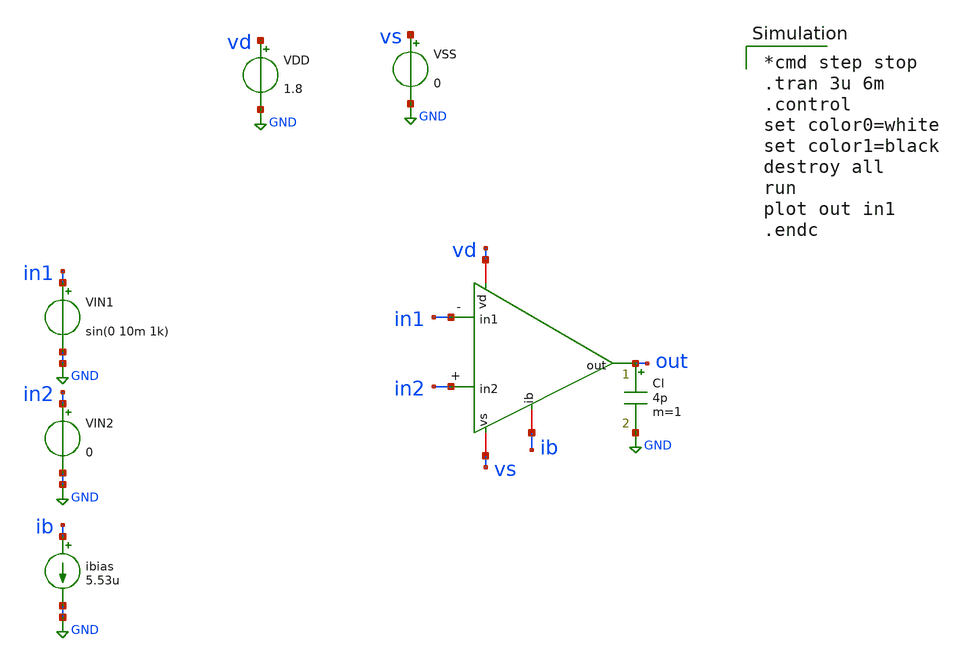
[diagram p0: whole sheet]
** sch_path: amp-op/xschem/ampop_tb-tran.sch
* Copyright 2020 Stefan Frederik Schippers
* Licensed under the Apache License, Version 2.0 (the "License");
* you may not use this file except in compliance with the License.
* You may obtain a copy of the License at
* https://www.apache.org/licenses/LICENSE-2.0
* Unless required by applicable law or agreed to in writing, software
* distributed under the License is distributed on an "AS IS" BASIS,
* WITHOUT WARRANTIES OR CONDITIONS OF ANY KIND, either express or implied.
* See the License for the specific language governing permissions and
* limitations under the License.
**.subckt ampop_tb-tran
VIN2 in2 GND 0
VIN1 in1 GND sin(0 10m 1k)
ibias ib GND 5.53u
VDD vd GND 1.8
VSS vs GND 0
Cl out GND 4p m=1
x1 vd in1 in2 out ib vs ampop
**** begin user architecture code

*cmd step stop
.tran 3u 6m
.control
set color0=white
set color1=black
destroy all
run
plot out in1
.endc

 .lib $::SKYWATER_MODELS/sky130.lib.spice tt
.include $::SKYWATER_STDCELLS/sky130_fd_sc_hd.spice

**** end user architecture code
**.ends

* expanding   symbol:  /home/hugodg/projects-sky130/temp-sensor/amp-op/xschem/ampop.sym # of pins=6
** sym_path: amp-op/xschem/ampop.sym
** sch_path: amp-op/xschem/ampop.sch
.subckt ampop vd in1 in2 out ib vs
*.iopin vd
*.opin out
*.ipin in1
*.ipin in2
*.iopin vs
*.iopin ib
X1 vd net1 out ib vs buffer
X2 vd ib net1 in2 in1 vs ota
**** begin user architecture code


R0 in1 in1.t0 88.243
R1 in2 in2.t0 88.786
R2 vs.n0 vs.n4 362.164
R3 vs.n0 vs.n2 362.164
R4 vs.n30 vs.n25 181.834
R5 vs.n14 vs.n9 181.834
R6 vs.n18 vs.n17 108.422
R7 vs.n31 vs.n30 108.422
R8 vs.n0 vs.n6 108.422
R9 vs.n15 vs.n14 108.422
R10 vs.n34 vs.n5 5.045
R11 vs.n5 vs 0.812
R12 vs vs 0.431
R13 vs.n34 vs.n33 0.202
R14 vs vs.n34 0.182
R15 vs.n19 vs.n16 0.15
R16 vs.n32 vs.n23 0.062
R17 vs.n20 vs.n19 0.057
R18 vs.n16 vs.n7 0.055
R19 vs.n25 vs.n24 0.046
R20 vs.n9 vs.n8 0.046
R21 vs.n30 vs.n29 0.042
R22 vs.n14 vs.n13 0.042
R23 vs.n28 vs.n27 0.035
R24 vs.n12 vs.n11 0.035
R25 vs.n27 vs.n26 0.025
R26 vs.n11 vs.n10 0.025
R27 vs.n29 vs.n28 0.025
R28 vs.n13 vs.n12 0.025
R29 vs.n16 vs.n15 0.017
R30 vs.n19 vs.n18 0.017
R31 vs.n32 vs.n31 0.017
R32 vs.n4 vs.n3 0.013
R33 vs.n2 vs.n1 0.013
R34 vs.n7 vs.n0 0.007
R35 vs vs 0.005
R36 vs.n23 vs.n20 0.004
R37 vs.n33 vs.n32 0.003
R38 vs.n5 vs 0.002
R39 vs.n22 vs.n21 0.001
R40 vs.n23 vs.n22 0.001
R41 ib.n5 ib.t6 196.205
R42 ib.n6 ib.t5 196.185
R43 ib.n7 ib.t8 196.183
R44 ib.n8 ib.t7 196.181
R45 ib.n4 ib.t2 160.591
R46 ib.t2 ib.n3 160.08
R47 ib.n4 ib.t4 160.055
R48 ib.n0 ib.t9 24.837
R49 ib.n0 ib.t0 24.107
R50 ib.n1 ib.t1 17.747
R51 ib.n3 ib.t3 5.789
R52 ib.n2 ib.n1 4.041
R53 ib ib.n8 3.3
R54 ib.n5 ib.n4 1.125
R55 ib.n3 ib 0.407
R56 ib.n1 ib.n0 0.387
R57 ib.n6 ib.n5 0.175
R58 ib.n8 ib.n7 0.168
R59 ib.n7 ib.n6 0.162
R60 ib.n2 ib 0.113
R61 ib ib.n2 0.078
R62 vd.n74 vd.n73 5396.47
R63 vd.n63 vd.n62 3501.18
R64 vd.n84 vd.n83 3501.18
R65 vd.n62 vd.n59 909.81
R66 vd.n83 vd.n80 909.81
R67 vd.n65 vd.n64 722.167
R68 vd.n86 vd.n85 722.167
R69 vd.n71 vd.n70 575.623
R70 vd.n75 vd.n70 575.623
R71 vd.n74 vd.n69 569.784
R72 vd.n72 vd.n71 515.374
R73 vd.n53 vd.n52 379.482
R74 vd.n40 vd.n34 379.482
R75 vd.n61 vd.n60 373.458
R76 vd.n65 vd.n60 373.458
R77 vd.n82 vd.n81 373.458
R78 vd.n86 vd.n81 373.458
R79 vd.n69 vd.n68 326.776
R80 vd.n54 vd.n53 297.411
R81 vd.n41 vd.n40 297.411
R82 vd.n59 vd.n58 270.305
R83 vd.n80 vd.n79 270.305
R84 vd.n76 vd.n75 251.205
R85 vd.n71 vd.n68 248.846
R86 vd.n19 vd.n16 131.387
R87 vd.n4 vd.n1 131.387
R88 vd.n24 vd.n21 131.011
R89 vd.n9 vd.n6 131.011
R90 vd.n66 vd.n65 105.107
R91 vd.n87 vd.n86 105.107
R92 vd.n61 vd.n58 103.152
R93 vd.n82 vd.n79 103.152
R94 vd.n29 vd.n24 54.211
R95 vd.n14 vd.n9 54.211
R96 vd.n29 vd.n19 53.835
R97 vd.n14 vd.n4 53.835
R98 vd.n57 vd.n14 8.271
R99 vd.n57 vd.n29 7.938
R100 vd.n57 vd.n56 4.028
R101 vd.n91 vd.n90 1.897
R102 vd.n77 vd.n76 1.606
R103 vd.n67 vd.n66 1.199
R104 vd.n88 vd.n87 1.199
R105 vd.n91 vd.n57 1.058
R106 vd vd.n89 1.008
R107 vd.n78 vd.n77 0.975
R108 vd vd.n88 0.594
R109 vd.n77 vd.n68 0.389
R110 vd.n67 vd.n58 0.389
R111 vd.n88 vd.n79 0.334
R112 vd.n55 vd.n45 0.296
R113 vd.n89 vd.n78 0.273
R114 vd.n42 vd.n32 0.228
R115 vd.n56 vd.n55 0.18
R116 vd.n89 vd 0.173
R117 vd.n56 vd.n42 0.167
R118 vd.n19 vd.n18 0.161
R119 vd.n24 vd.n23 0.161
R120 vd.n4 vd.n3 0.161
R121 vd.n9 vd.n8 0.161
R122 vd.n23 vd.n22 0.139
R123 vd.n8 vd.n7 0.139
R124 vd.n18 vd.n17 0.139
R125 vd.n3 vd.n2 0.139
R126 vd.n90 vd 0.071
R127 vd.n78 vd.n67 0.054
R128 vd vd.n91 0.044
R129 vd.n90 vd 0.034
R130 vd.n42 vd.n41 0.017
R131 vd.n55 vd.n54 0.017
R132 vd.n62 vd.n61 0.015
R133 vd.n83 vd.n82 0.015
R134 vd.n16 vd.n15 0.015
R135 vd.n21 vd.n20 0.015
R136 vd.n1 vd.n0 0.015
R137 vd.n6 vd.n5 0.015
R138 vd.n52 vd.n51 0.013
R139 vd.n34 vd.n33 0.013
R140 vd.n26 vd.n25 0.013
R141 vd.n27 vd.n26 0.013
R142 vd.n11 vd.n10 0.013
R143 vd.n12 vd.n11 0.013
R144 vd.n75 vd.n74 0.004
R145 vd.n73 vd.n72 0.003
R146 vd.n63 vd.n60 0.003
R147 vd.n84 vd.n81 0.003
R148 vd.n53 vd.n50 0.003
R149 vd.n47 vd.n46 0.003
R150 vd.n36 vd.n35 0.003
R151 vd.n40 vd.n39 0.003
R152 vd.n64 vd.n63 0.003
R153 vd.n85 vd.n84 0.003
R154 vd.n50 vd.n49 0.003
R155 vd.n37 vd.n36 0.003
R156 vd.n48 vd.n47 0.003
R157 vd.n39 vd.n38 0.003
R158 vd.n73 vd.n70 0.003
R159 vd.n49 vd.n48 0.002
R160 vd.n38 vd.n37 0.002
R161 vd.n29 vd.n28 0.002
R162 vd.n28 vd.n27 0.002
R163 vd.n14 vd.n13 0.002
R164 vd.n13 vd.n12 0.002
R165 vd.n72 vd.n69 0.001
R166 vd.n64 vd.n59 0.001
R167 vd.n85 vd.n80 0.001
R168 vd.n32 vd.n31 0.001
R169 vd.n45 vd.n44 0.001
R170 vd.n44 vd.n43 0.001
R171 vd.n31 vd.n30 0.001
R172 vd.n76 vd.n69 0.001
R173 vd.n66 vd.n59 0.001
R174 vd.n87 vd.n80 0.001
R175 out.t0 out.n7 175.091
R176 out.n0 out.t2 175.044
R177 out.n2 out.n1 150.491
R178 out.n4 out.n3 150.491
R179 out.n6 out.n5 141.106
R180 out out.t0 28.743
R181 out.n5 out.t1 24.103
R182 out.n6 out.t7 24.103
R183 out.n4 out.t5 24.103
R184 out.n2 out.t3 24.102
R185 out.n0 out.t6 24.102
R186 out.n1 out.t9 24.102
R187 out.n3 out.t4 24.102
R188 out.n7 out.t8 24.102
R189 out.n7 out.n6 1.085
R190 out.n3 out.n2 0.988
R191 out.n5 out.n4 0.913
R192 out.n1 out.n0 0.863
R193 out out 0.023
R194 buffer_0/net1.n4 buffer_0/net1.t29 172.218
R195 buffer_0/net1.n5 buffer_0/net1.n4 149.523
R196 buffer_0/net1.n6 buffer_0/net1.n5 149.523
R197 buffer_0/net1.n7 buffer_0/net1.n6 149.523
R198 buffer_0/net1.n8 buffer_0/net1.n7 149.523
R199 buffer_0/net1.n9 buffer_0/net1.n8 149.523
R200 buffer_0/net1.n10 buffer_0/net1.n9 149.523
R201 buffer_0/net1.n11 buffer_0/net1.n10 149.523
R202 buffer_0/net1.n12 buffer_0/net1.n11 149.523
R203 buffer_0/net1.n13 buffer_0/net1.n12 149.523
R204 buffer_0/net1.n14 buffer_0/net1.n13 149.523
R205 buffer_0/net1.n15 buffer_0/net1.n14 149.523
R206 buffer_0/net1.n16 buffer_0/net1.n15 149.523
R207 buffer_0/net1.n17 buffer_0/net1.n16 149.523
R208 buffer_0/net1.n18 buffer_0/net1.n17 149.523
R209 buffer_0/net1.n19 buffer_0/net1.n18 149.523
R210 buffer_0/net1.n20 buffer_0/net1.n19 149.523
R211 buffer_0/net1.n21 buffer_0/net1.n20 149.523
R212 buffer_0/net1.n22 buffer_0/net1.n21 148.639
R213 buffer_0/net1.n22 buffer_0/net1.t16 24.284
R214 buffer_0/net1.n21 buffer_0/net1.t10 24.101
R215 buffer_0/net1.n20 buffer_0/net1.t27 24.101
R216 buffer_0/net1.n19 buffer_0/net1.t21 24.101
R217 buffer_0/net1.n18 buffer_0/net1.t4 24.101
R218 buffer_0/net1.n17 buffer_0/net1.t0 24.101
R219 buffer_0/net1.n16 buffer_0/net1.t22 24.101
R220 buffer_0/net1.n15 buffer_0/net1.t26 24.101
R221 buffer_0/net1.n14 buffer_0/net1.t18 24.101
R222 buffer_0/net1.n13 buffer_0/net1.t6 24.101
R223 buffer_0/net1.n12 buffer_0/net1.t23 24.101
R224 buffer_0/net1.n11 buffer_0/net1.t25 24.101
R225 buffer_0/net1.n10 buffer_0/net1.t8 24.101
R226 buffer_0/net1.n9 buffer_0/net1.t12 24.101
R227 buffer_0/net1.n8 buffer_0/net1.t28 24.101
R228 buffer_0/net1.n7 buffer_0/net1.t24 24.101
R229 buffer_0/net1.n6 buffer_0/net1.t14 24.101
R230 buffer_0/net1.n5 buffer_0/net1.t2 24.101
R231 buffer_0/net1.n4 buffer_0/net1.t20 24.101
R232 buffer_0/net1.n3 buffer_0/net1.t11 17.4
R233 buffer_0/net1.n3 buffer_0/net1.t17 17.4
R234 buffer_0/net1.n0 buffer_0/net1.t3 17.4
R235 buffer_0/net1.n0 buffer_0/net1.t15 17.4
R236 buffer_0/net1.n1 buffer_0/net1.t13 17.4
R237 buffer_0/net1.n1 buffer_0/net1.t9 17.4
R238 buffer_0/net1.n2 buffer_0/net1.t1 17.4
R239 buffer_0/net1.n2 buffer_0/net1.t5 17.4
R240 buffer_0/net1.n25 buffer_0/net1.t7 17.4
R241 buffer_0/net1.n25 buffer_0/net1.t19 17.4
R242 buffer_0/net1.n24 buffer_0/net1.n23 3.481
R243 buffer_0/net1 buffer_0/net1.n0 3.306
R244 buffer_0/net1.n27 buffer_0/net1.n26 3.218
R245 buffer_0/net1.n26 buffer_0/net1.n24 3.218
R246 buffer_0/net1.n23 buffer_0/net1.n22 1.24
R247 buffer_0/net1.n27 buffer_0/net1.n1 0.931
R248 buffer_0/net1.n24 buffer_0/net1.n2 0.931
R249 buffer_0/net1.n26 buffer_0/net1.n25 0.931
R250 buffer_0/net1 buffer_0/net1.n27 0.843
R251 buffer_0/net1.n23 buffer_0/net1.n3 0.389
C0 ota_0/m1_1300_5200# ota_0/out -0.03fF
C1 buffer_0/net2 vd 0.01fF
C2 ota_0/out vd 0.05fF
C3 buffer_0/net1.t3 vs 0.02fF
C4 buffer_0/net1.t15 vs 0.02fF
C5 buffer_0/net1.n0 vs 0.31fF $ **FLOATING
C6 buffer_0/net1.t13 vs 0.02fF
C7 buffer_0/net1.t9 vs 0.02fF
C8 buffer_0/net1.n1 vs 0.19fF $ **FLOATING
C9 buffer_0/net1.t1 vs 0.02fF
C10 buffer_0/net1.t5 vs 0.02fF
C11 buffer_0/net1.n2 vs 0.19fF $ **FLOATING
C12 buffer_0/net1.t11 vs 0.02fF
C13 buffer_0/net1.t17 vs 0.02fF
C14 buffer_0/net1.n3 vs 0.15fF $ **FLOATING
C15 buffer_0/net1.t10 vs 0.47fF
C16 buffer_0/net1.t27 vs 0.47fF
C17 buffer_0/net1.t21 vs 0.47fF
C18 buffer_0/net1.t4 vs 0.47fF
C19 buffer_0/net1.t0 vs 0.47fF
C20 buffer_0/net1.t22 vs 0.47fF
C21 buffer_0/net1.t26 vs 0.47fF
C22 buffer_0/net1.t18 vs 0.47fF
C23 buffer_0/net1.t6 vs 0.47fF
C24 buffer_0/net1.t23 vs 0.47fF
C25 buffer_0/net1.t25 vs 0.47fF
C26 buffer_0/net1.t8 vs 0.47fF
C27 buffer_0/net1.t12 vs 0.47fF
C28 buffer_0/net1.t28 vs 0.47fF
C29 buffer_0/net1.t24 vs 0.47fF
C30 buffer_0/net1.t14 vs 0.47fF
C31 buffer_0/net1.t2 vs 0.47fF
C32 buffer_0/net1.t20 vs 0.47fF
C33 buffer_0/net1.t29 vs 0.75fF
C34 buffer_0/net1.n4 vs 0.39fF $ **FLOATING
C35 buffer_0/net1.n5 vs 0.34fF $ **FLOATING
C36 buffer_0/net1.n6 vs 0.34fF $ **FLOATING
C37 buffer_0/net1.n7 vs 0.34fF $ **FLOATING
C38 buffer_0/net1.n8 vs 0.34fF $ **FLOATING
C39 buffer_0/net1.n9 vs 0.34fF $ **FLOATING
C40 buffer_0/net1.n10 vs 0.34fF $ **FLOATING
C41 buffer_0/net1.n11 vs 0.34fF $ **FLOATING
C42 buffer_0/net1.n12 vs 0.34fF $ **FLOATING
C43 buffer_0/net1.n13 vs 0.34fF $ **FLOATING
C44 buffer_0/net1.n14 vs 0.34fF $ **FLOATING
C45 buffer_0/net1.n15 vs 0.34fF $ **FLOATING
C46 buffer_0/net1.n16 vs 0.34fF $ **FLOATING
C47 buffer_0/net1.n17 vs 0.34fF $ **FLOATING
C48 buffer_0/net1.n18 vs 0.34fF $ **FLOATING
C49 buffer_0/net1.n19 vs 0.34fF $ **FLOATING
C50 buffer_0/net1.n20 vs 0.34fF $ **FLOATING
C51 buffer_0/net1.n21 vs 0.34fF $ **FLOATING
C52 buffer_0/net1.t16 vs 0.47fF
C53 buffer_0/net1.n22 vs 0.21fF $ **FLOATING
C54 buffer_0/net1.n23 vs 1.22fF $ **FLOATING
C55 buffer_0/net1.n24 vs 4.35fF $ **FLOATING
C56 buffer_0/net1.t7 vs 0.02fF
C57 buffer_0/net1.t19 vs 0.02fF
C58 buffer_0/net1.n25 vs 0.19fF $ **FLOATING
C59 buffer_0/net1.n26 vs 0.36fF $ **FLOATING
C60 buffer_0/net1.n27 vs 0.25fF $ **FLOATING
C61 out.t8 vs 0.59fF
C62 out.t1 vs 0.59fF
C63 out.t4 vs 0.59fF
C64 out.t9 vs 0.59fF
C65 out.t2 vs 0.94fF
C66 out.t6 vs 0.59fF
C67 out.n0 vs 2.69fF $ **FLOATING
C68 out.n1 vs 2.83fF $ **FLOATING
C69 out.t3 vs 0.59fF
C70 out.n2 vs 0.86fF $ **FLOATING
C71 out.n3 vs 0.86fF $ **FLOATING
C72 out.t5 vs 0.59fF
C73 out.n4 vs 0.91fF $ **FLOATING
C74 out.n5 vs 0.92fF $ **FLOATING
C75 out.t7 vs 0.59fF
C76 out.n6 vs 0.84fF $ **FLOATING
C77 out.n7 vs 0.91fF $ **FLOATING
C78 out.t0 vs 0.89fF
C79 vd.n0 vs 0.34fF $ **FLOATING
C80 vd.n1 vs 0.06fF $ **FLOATING
C81 vd.n2 vs 0.33fF $ **FLOATING
C82 vd.n3 vs 0.04fF $ **FLOATING
C83 vd.n4 vs 0.04fF $ **FLOATING
C84 vd.n5 vs 0.34fF $ **FLOATING
C85 vd.n6 vs 0.06fF $ **FLOATING
C86 vd.n7 vs 0.33fF $ **FLOATING
C87 vd.n8 vs 0.04fF $ **FLOATING
C88 vd.n9 vs 0.04fF $ **FLOATING
C89 vd.n10 vs 0.07fF $ **FLOATING
C90 vd.n11 vs 0.07fF $ **FLOATING
C91 vd.n12 vs 0.35fF $ **FLOATING
C92 vd.n13 vs 0.02fF $ **FLOATING
C93 vd.n14 vs 0.49fF $ **FLOATING
C94 vd.n15 vs 0.34fF $ **FLOATING
C95 vd.n16 vs 0.06fF $ **FLOATING
C96 vd.n17 vs 0.33fF $ **FLOATING
C97 vd.n18 vs 0.04fF $ **FLOATING
C98 vd.n19 vs 0.04fF $ **FLOATING
C99 vd.n20 vs 0.34fF $ **FLOATING
C100 vd.n21 vs 0.06fF $ **FLOATING
C101 vd.n22 vs 0.33fF $ **FLOATING
C102 vd.n23 vs 0.04fF $ **FLOATING
C103 vd.n24 vs 0.04fF $ **FLOATING
C104 vd.n25 vs 0.07fF $ **FLOATING
C105 vd.n26 vs 0.07fF $ **FLOATING
C106 vd.n27 vs 0.35fF $ **FLOATING
C107 vd.n28 vs 0.02fF $ **FLOATING
C108 vd.n29 vs 0.51fF $ **FLOATING
C109 vd.n30 vs 1.30fF $ **FLOATING
C110 vd.n31 vs 0.03fF $ **FLOATING
C111 vd.n32 vs 0.64fF $ **FLOATING
C112 vd.n33 vs 1.30fF $ **FLOATING
C113 vd.n34 vs 0.15fF $ **FLOATING
C114 vd.n35 vs 0.13fF $ **FLOATING
C115 vd.n36 vs 0.14fF $ **FLOATING
C116 vd.n37 vs 1.01fF $ **FLOATING
C117 vd.n38 vs 1.01fF $ **FLOATING
C118 vd.n39 vs 0.14fF $ **FLOATING
C119 vd.n40 vs 0.13fF $ **FLOATING
C120 vd.n41 vs 0.07fF $ **FLOATING
C121 vd.n42 vs 0.10fF $ **FLOATING
C122 vd.n43 vs 1.30fF $ **FLOATING
C123 vd.n44 vs 0.03fF $ **FLOATING
C124 vd.n45 vs 0.34fF $ **FLOATING
C125 vd.n46 vs 0.13fF $ **FLOATING
C126 vd.n47 vs 0.14fF $ **FLOATING
C127 vd.n48 vs 1.01fF $ **FLOATING
C128 vd.n49 vs 1.01fF $ **FLOATING
C129 vd.n50 vs 0.14fF $ **FLOATING
C130 vd.n51 vs 1.30fF $ **FLOATING
C131 vd.n52 vs 0.15fF $ **FLOATING
C132 vd.n53 vs 0.13fF $ **FLOATING
C133 vd.n54 vs 0.07fF $ **FLOATING
C134 vd.n55 vs 0.35fF $ **FLOATING
C135 vd.n56 vs 1.41fF $ **FLOATING
C136 vd.n57 vs 13.41fF $ **FLOATING
C137 vd.n58 vs 0.09fF $ **FLOATING
C138 vd.n59 vs 2.13fF $ **FLOATING
C139 vd.n60 vs 0.14fF $ **FLOATING
C140 vd.n61 vs 0.09fF $ **FLOATING
C141 vd.n62 vs 1.22fF $ **FLOATING
C142 vd.n63 vs 0.14fF $ **FLOATING
C143 vd.n65 vs 1.31fF $ **FLOATING
C144 vd.n66 vs 0.26fF $ **FLOATING
C145 vd.n67 vs 0.81fF $ **FLOATING
C146 vd.n68 vs 0.13fF $ **FLOATING
C147 vd.n69 vs 5.56fF $ **FLOATING
C148 vd.n70 vs 0.22fF $ **FLOATING
C149 vd.n71 vs 3.29fF $ **FLOATING
C150 vd.n73 vs 0.22fF $ **FLOATING
C151 vd.n74 vs 3.13fF $ **FLOATING
C152 vd.n75 vs 0.16fF $ **FLOATING
C153 vd.n76 vs 0.34fF $ **FLOATING
C154 vd.n77 vs 3.07fF $ **FLOATING
C155 vd.n78 vs 0.50fF $ **FLOATING
C156 vd.n79 vs 0.09fF $ **FLOATING
C157 vd.n80 vs 2.13fF $ **FLOATING
C158 vd.n81 vs 0.14fF $ **FLOATING
C159 vd.n82 vs 0.09fF $ **FLOATING
C160 vd.n83 vs 1.22fF $ **FLOATING
C161 vd.n84 vs 0.14fF $ **FLOATING
C162 vd.n86 vs 1.31fF $ **FLOATING
C163 vd.n87 vs 0.26fF $ **FLOATING
C164 vd.n88 vs 1.13fF $ **FLOATING
C165 vd.n89 vs 1.25fF $ **FLOATING
C166 vd.n90 vs 1.36fF $ **FLOATING
C167 vd.n91 vs 1.49fF $ **FLOATING
C168 ib.t1 vs 0.01fF
C169 ib.t9 vs 0.19fF
C170 ib.t0 vs 0.19fF
C171 ib.n0 vs 0.26fF $ **FLOATING
C172 ib.n1 vs 0.16fF $ **FLOATING
C173 ib.n2 vs 0.12fF $ **FLOATING
C174 ib.t8 vs 0.81fF
C175 ib.t5 vs 0.81fF
C176 ib.t6 vs 0.81fF
C177 ib.t4 vs 0.68fF
C178 ib.t3 vs 0.12fF
C179 ib.n3 vs 1.03fF $ **FLOATING
C180 ib.t2 vs 0.41fF
C181 ib.n4 vs 1.75fF $ **FLOATING
C182 ib.n5 vs 0.99fF $ **FLOATING
C183 ib.n6 vs 0.51fF $ **FLOATING
C184 ib.n7 vs 0.52fF $ **FLOATING
C185 ib.t7 vs 0.81fF
C186 ib.n8 vs 1.32fF $ **FLOATING
C187 buffer_0/net4 vs 1.11fF
C188 out vs 13.18fF
C189 buffer_0/net3 vs 2.90fF
C190 vd vs 38.03fF
C191 buffer_0/net1 vs 14.70fF
C192 buffer_0/net2 vs 3.06fF
C193 ota_0/out vs 11.16fF
C194 ota_0/m1_n20_5200# vs 2.40fF
C195 ota_0/m1_420_6300# vs 4.72fF
C196 ota_0/m1_1300_5200# vs 14.02fF


**** end user architecture code
.ends


* expanding   symbol:  /home/hugodg/projects-sky130/temp-sensor/amp-op/xschem/buffer.sym # of pins=5
** sym_path: buffer/xschem/buffer.sym
** sch_path: buffer/xschem/buffer.sch
.subckt buffer vd in out ib gnd
*.iopin vd
*.iopin ib
*.iopin out
*.iopin in
*.iopin gnd
XM3 net2 net2 vd vd sky130_fd_pr__pfet_01v8 L=1 W=1 nf=1 ad='int((nf+1)/2) * W/nf * 0.29' as='int((nf+2)/2) * W/nf * 0.29'
+ pd='2*int((nf+1)/2) * (W/nf + 0.29)' ps='2*int((nf+2)/2) * (W/nf + 0.29)' nrd='0.29 / W' nrs='0.29 / W'
+ sa=0 sb=0 sd=0 mult=1 m=1
XM1 net2 out net4 gnd sky130_fd_pr__nfet_01v8 L=1 W=10 nf=10 ad='int((nf+1)/2) * W/nf * 0.29' as='int((nf+2)/2) * W/nf * 0.29'
+ pd='2*int((nf+1)/2) * (W/nf + 0.29)' ps='2*int((nf+2)/2) * (W/nf + 0.29)' nrd='0.29 / W' nrs='0.29 / W'
+ sa=0 sb=0 sd=0 mult=1 m=1
XM2 net3 in net4 gnd sky130_fd_pr__nfet_01v8 L=1 W=10 nf=10 ad='int((nf+1)/2) * W/nf * 0.29' as='int((nf+2)/2) * W/nf * 0.29'
+ pd='2*int((nf+1)/2) * (W/nf + 0.29)' ps='2*int((nf+2)/2) * (W/nf + 0.29)' nrd='0.29 / W' nrs='0.29 / W'
+ sa=0 sb=0 sd=0 mult=1 m=1
XM4 net3 net3 vd vd sky130_fd_pr__pfet_01v8 L=1 W=1 nf=1 ad='int((nf+1)/2) * W/nf * 0.29' as='int((nf+2)/2) * W/nf * 0.29'
+ pd='2*int((nf+1)/2) * (W/nf + 0.29)' ps='2*int((nf+2)/2) * (W/nf + 0.29)' nrd='0.29 / W' nrs='0.29 / W'
+ sa=0 sb=0 sd=0 mult=1 m=1
XM5 net4 ib gnd gnd sky130_fd_pr__nfet_01v8 L=1 W=1 nf=1 ad='int((nf+1)/2) * W/nf * 0.29' as='int((nf+2)/2) * W/nf * 0.29'
+ pd='2*int((nf+1)/2) * (W/nf + 0.29)' ps='2*int((nf+2)/2) * (W/nf + 0.29)' nrd='0.29 / W' nrs='0.29 / W'
+ sa=0 sb=0 sd=0 mult=1 m=1
XM6 out net3 vd vd sky130_fd_pr__pfet_01v8 L=1 W=10 nf=10 ad='int((nf+1)/2) * W/nf * 0.29' as='int((nf+2)/2) * W/nf * 0.29'
+ pd='2*int((nf+1)/2) * (W/nf + 0.29)' ps='2*int((nf+2)/2) * (W/nf + 0.29)' nrd='0.29 / W' nrs='0.29 / W'
+ sa=0 sb=0 sd=0 mult=1 m=1
XM7 out net1 gnd gnd sky130_fd_pr__nfet_01v8 L=1 W=10 nf=10 ad='int((nf+1)/2) * W/nf * 0.29' as='int((nf+2)/2) * W/nf * 0.29'
+ pd='2*int((nf+1)/2) * (W/nf + 0.29)' ps='2*int((nf+2)/2) * (W/nf + 0.29)' nrd='0.29 / W' nrs='0.29 / W'
+ sa=0 sb=0 sd=0 mult=1 m=1
XM8 net1 net2 vd vd sky130_fd_pr__pfet_01v8 L=1 W=10 nf=10 ad='int((nf+1)/2) * W/nf * 0.29' as='int((nf+2)/2) * W/nf * 0.29'
+ pd='2*int((nf+1)/2) * (W/nf + 0.29)' ps='2*int((nf+2)/2) * (W/nf + 0.29)' nrd='0.29 / W' nrs='0.29 / W'
+ sa=0 sb=0 sd=0 mult=1 m=1
XM9 net1 net1 gnd gnd sky130_fd_pr__nfet_01v8 L=1 W=10 nf=10 ad='int((nf+1)/2) * W/nf * 0.29' as='int((nf+2)/2) * W/nf * 0.29'
+ pd='2*int((nf+1)/2) * (W/nf + 0.29)' ps='2*int((nf+2)/2) * (W/nf + 0.29)' nrd='0.29 / W' nrs='0.29 / W'
+ sa=0 sb=0 sd=0 mult=1 m=1
XM10 ib ib gnd gnd sky130_fd_pr__nfet_01v8 L=1 W=1 nf=1 ad='int((nf+1)/2) * W/nf * 0.29' as='int((nf+2)/2) * W/nf * 0.29'
+ pd='2*int((nf+1)/2) * (W/nf + 0.29)' ps='2*int((nf+2)/2) * (W/nf + 0.29)' nrd='0.29 / W' nrs='0.29 / W'
+ sa=0 sb=0 sd=0 mult=1 m=1
XPD1 net8 net7 net6 net5 sky130_fd_pr__pfet_01v8 L=1 W=1 nf=1 ad='int((nf+1)/2) * W/nf * 0.29' as='int((nf+2)/2) * W/nf * 0.29'
+ pd='2*int((nf+1)/2) * (W/nf + 0.29)' ps='2*int((nf+2)/2) * (W/nf + 0.29)' nrd='0.29 / W' nrs='0.29 / W'
+ sa=0 sb=0 sd=0 mult=1 m=1
XPD2 net12 net11 net10 net9 sky130_fd_pr__pfet_01v8 L=1 W=1 nf=1 ad='int((nf+1)/2) * W/nf * 0.29' as='int((nf+2)/2) * W/nf * 0.29'
+ pd='2*int((nf+1)/2) * (W/nf + 0.29)' ps='2*int((nf+2)/2) * (W/nf + 0.29)' nrd='0.29 / W' nrs='0.29 / W'
+ sa=0 sb=0 sd=0 mult=1 m=1
XPD3 net16 net15 net14 net13 sky130_fd_pr__pfet_01v8 L=1 W=1 nf=1 ad='int((nf+1)/2) * W/nf * 0.29' as='int((nf+2)/2) * W/nf * 0.29'
+ pd='2*int((nf+1)/2) * (W/nf + 0.29)' ps='2*int((nf+2)/2) * (W/nf + 0.29)' nrd='0.29 / W' nrs='0.29 / W'
+ sa=0 sb=0 sd=0 mult=1 m=1
XPD4 net20 net19 net18 net17 sky130_fd_pr__pfet_01v8 L=1 W=1 nf=1 ad='int((nf+1)/2) * W/nf * 0.29' as='int((nf+2)/2) * W/nf * 0.29'
+ pd='2*int((nf+1)/2) * (W/nf + 0.29)' ps='2*int((nf+2)/2) * (W/nf + 0.29)' nrd='0.29 / W' nrs='0.29 / W'
+ sa=0 sb=0 sd=0 mult=1 m=1
XND1 net25 net21 net26 gnd sky130_fd_pr__nfet_01v8 L=1 W=1 nf=1 ad='int((nf+1)/2) * W/nf * 0.29' as='int((nf+2)/2) * W/nf * 0.29'
+ pd='2*int((nf+1)/2) * (W/nf + 0.29)' ps='2*int((nf+2)/2) * (W/nf + 0.29)' nrd='0.29 / W' nrs='0.29 / W'
+ sa=0 sb=0 sd=0 mult=1 m=1
XND2 net27 net22 net28 gnd sky130_fd_pr__nfet_01v8 L=1 W=1 nf=1 ad='int((nf+1)/2) * W/nf * 0.29' as='int((nf+2)/2) * W/nf * 0.29'
+ pd='2*int((nf+1)/2) * (W/nf + 0.29)' ps='2*int((nf+2)/2) * (W/nf + 0.29)' nrd='0.29 / W' nrs='0.29 / W'
+ sa=0 sb=0 sd=0 mult=1 m=1
XND3 net29 net23 net30 gnd sky130_fd_pr__nfet_01v8 L=1 W=1 nf=1 ad='int((nf+1)/2) * W/nf * 0.29' as='int((nf+2)/2) * W/nf * 0.29'
+ pd='2*int((nf+1)/2) * (W/nf + 0.29)' ps='2*int((nf+2)/2) * (W/nf + 0.29)' nrd='0.29 / W' nrs='0.29 / W'
+ sa=0 sb=0 sd=0 mult=1 m=1
XND4 net32 net24 net31 gnd sky130_fd_pr__nfet_01v8 L=1 W=1 nf=1 ad='int((nf+1)/2) * W/nf * 0.29' as='int((nf+2)/2) * W/nf * 0.29'
+ pd='2*int((nf+1)/2) * (W/nf + 0.29)' ps='2*int((nf+2)/2) * (W/nf + 0.29)' nrd='0.29 / W' nrs='0.29 / W'
+ sa=0 sb=0 sd=0 mult=1 m=1
.ends


* expanding   symbol:  /home/hugodg/projects-sky130/temp-sensor/amp-op/xschem/ota.sym # of pins=6
** sym_path: amp-op/xschem/ota.sym
** sch_path: amp-op/xschem/ota.sch
.subckt ota vd ib out in2 in1 vs
*.iopin vd
*.iopin vs
*.iopin ib
*.ipin in1
*.ipin in2
*.opin out
XCC out d sky130_fd_pr__cap_mim_m3_1 W=21 L=21 MF=1 m=1
**** begin user architecture code


RR0 vs.n20 vs.n14 202.916
R1 vs.n7 vs.n1 202.916
R2 vs.n21 vs.n20 121.975
R3 vs.n8 vs.n7 121.975
R4 vs.n28 vs.n27 2.673
R5 vs.n29 vs.n28 1.458
R6 vs vs.n29 1.104
R7 vs.n27 vs.n26 0.911
R8 vs.n25 vs.n24 0.348
R9 vs.n12 vs.n11 0.348
R10 vs.n28 vs.n25 0.135
R11 vs.n29 vs.n12 0.135
R12 vs.n25 vs.n21 0.09
R13 vs.n12 vs.n8 0.09
R14 vs.n14 vs.n13 0.04
R15 vs.n1 vs.n0 0.04
R16 vs.n18 vs.n17 0.037
R17 vs.n5 vs.n4 0.037
R18 vs.n16 vs.n15 0.034
R19 vs.n20 vs.n19 0.034
R20 vs.n3 vs.n2 0.034
R21 vs.n7 vs.n6 0.034
R22 vs.n17 vs.n16 0.016
R23 vs.n4 vs.n3 0.016
R24 vs.n19 vs.n18 0.016
R25 vs.n6 vs.n5 0.016
R26 vs.n24 vs.n23 0.001
R27 vs.n11 vs.n10 0.001
R28 vs.n23 vs.n22 0.001
R29 vs.n10 vs.n9 0.001
R30 out.n10 out.n4 394.54
R31 out.n11 out.n10 313.599
R32 out.n12 out.n2 0.386
R33 out out.n12 0.168
R34 out.n12 out.n11 0.052
R35 out.n4 out.n3 0.013
R36 out.n8 out.n7 0.003
R37 out.n6 out.n5 0.003
R38 out.n10 out.n9 0.003
R39 out.n7 out.n6 0.002
R40 out.n9 out.n8 0.002
R41 out.n2 out.n1 0.001
R42 out.n1 out.n0 0.001
R43 in1 in1.t0 88.743
R44 in2 in2.t0 90.145
R45 ib.n3 ib.t5 196.178
R46 ib.n2 ib.t3 196.178
R47 ib.n1 ib.t4 196.178
R48 ib.n0 ib.t6 196.178
R49 ib.n0 ib.t7 162.082
R50 ib.n5 ib.t0 160.028
R51 ib.n4 ib.t2 160.028
R52 ib.n6 ib.t1 6.282
R53 ib.n4 ib.n3 2.041
R54 ib.n5 ib.n4 2.041
R55 ib ib.n6 1.518
R56 ib.n1 ib.n0 0.537
R57 ib.n2 ib.n1 0.537
R58 ib.n3 ib.n2 0.537
R59 ib.n6 ib.n5 0.266
R60 vd.n5 vd.n1 507.374
R61 vd.n32 vd.n26 394.54
R62 vd.n19 vd.n13 394.54
R63 vd.n44 vd.n43 394.54
R64 vd.n7 vd.n6 331.818
R65 vd.n33 vd.n32 313.599
R66 vd.n20 vd.n19 313.599
R67 vd.n45 vd.n44 313.599
R68 vd vd.n49 3.951
R69 vd.n35 vd.n34 2.876
R70 vd.n8 vd.n7 1.417
R71 vd.n36 vd.n35 1.333
R72 vd.n35 vd.n21 0.835
R73 vd.n34 vd.n24 0.386
R74 vd.n21 vd.n11 0.386
R75 vd.n49 vd.n48 0.376
R76 vd vd.n36 0.229
R77 vd.n36 vd.n8 0.211
R78 vd.n49 vd.n45 0.063
R79 vd.n34 vd.n33 0.052
R80 vd.n21 vd.n20 0.052
R81 vd.n26 vd.n25 0.013
R82 vd.n13 vd.n12 0.013
R83 vd.n43 vd.n42 0.013
R84 vd.n6 vd.n5 0.004
R85 vd.n1 vd.n0 0.004
R86 vd.n30 vd.n29 0.003
R87 vd.n17 vd.n16 0.003
R88 vd.n40 vd.n39 0.003
R89 vd.n28 vd.n27 0.003
R90 vd.n32 vd.n31 0.003
R91 vd.n15 vd.n14 0.003
R92 vd.n19 vd.n18 0.003
R93 vd.n44 vd.n41 0.003
R94 vd.n38 vd.n37 0.003
R95 vd.n29 vd.n28 0.002
R96 vd.n16 vd.n15 0.002
R97 vd.n41 vd.n40 0.002
R98 vd.n31 vd.n30 0.002
R99 vd.n18 vd.n17 0.002
R100 vd.n39 vd.n38 0.002
R101 vd.n4 vd.n3 0.002
R102 vd.n3 vd.n2 0.002
R103 vd.n5 vd.n4 0.002
R104 vd.n48 vd.n47 0.001
R105 vd.n24 vd.n23 0.001
R106 vd.n11 vd.n10 0.001
R107 vd.n23 vd.n22 0.001
R108 vd.n10 vd.n9 0.001
R109 vd.n47 vd.n46 0.001
C0 w_460_9160# vs 0.25fF
C1 vs out 0.29fF
C2 vs e 0.43fF
C3 in2 in1 0.06fF
C4 w_460_9160# vd 0.57fF
C5 in2 d 0.06fF
C6 vd out 0.34fF
C7 vs c 0.57fF
C8 w_460_9160# ib 0.42fF
C9 ib out 0.09fF
C10 vd e 1.05fF
C11 ib e 0.91fF
C12 vd c 0.00fF
C13 ib c 0.01fF
C14 vs vd 0.07fF
C15 w_460_9160# in1 0.18fF
C16 vs ib 0.06fF
C17 w_460_9160# d 0.31fF
C18 out d 0.01fF
C19 e d 0.26fF
C20 ib vd 2.28fF
C21 in1 c 0.25fF
C22 c d 0.13fF
C23 in1 vs 0.08fF
C24 in2 w_460_9160# 0.53fF
C25 vs d 0.55fF
C26 in1 vd 0.01fF
C27 vd d 0.01fF
C28 in1 ib 0.03fF
C29 in2 c 0.07fF
C30 ib d 0.04fF
C31 in2 vs 0.05fF
C32 w_460_9160# e 0.07fF
C33 in2 vd 0.02fF
C34 e out 0.05fF
C35 in2 ib 0.20fF
C36 in1 d 0.01fF
C37 w_460_9160# c 0.56fF
C38 c e 0.00fF
C39 w_460_9160# 0 7.23fF
C40 vd.n0 0 0.19fF $ **FLOATING
C41 vd.n1 0 3.35fF $ **FLOATING
C42 vd.n2 0 0.16fF $ **FLOATING
C43 vd.n3 0 0.33fF $ **FLOATING
C44 vd.n4 0 2.51fF $ **FLOATING
C45 vd.n5 0 2.68fF $ **FLOATING
C46 vd.n6 0 0.32fF $ **FLOATING
C47 vd.n7 0 3.66fF $ **FLOATING
C48 vd.n8 0 2.18fF $ **FLOATING
C49 vd.n9 0 1.48fF $ **FLOATING
C50 vd.n10 0 0.03fF $ **FLOATING
C51 vd.n11 0 0.12fF $ **FLOATING
C52 vd.n12 0 1.48fF $ **FLOATING
C53 vd.n13 0 0.13fF $ **FLOATING
C54 vd.n14 0 0.11fF $ **FLOATING
C55 vd.n15 0 0.22fF $ **FLOATING
C56 vd.n16 0 1.02fF $ **FLOATING
C57 vd.n17 0 1.02fF $ **FLOATING
C58 vd.n18 0 0.22fF $ **FLOATING
C59 vd.n19 0 0.11fF $ **FLOATING
C60 vd.n20 0 0.07fF $ **FLOATING
C61 vd.n21 0 0.70fF $ **FLOATING
C62 vd.n22 0 1.48fF $ **FLOATING
C63 vd.n23 0 0.03fF $ **FLOATING
C64 vd.n24 0 0.12fF $ **FLOATING
C65 vd.n25 0 1.48fF $ **FLOATING
C66 vd.n26 0 0.13fF $ **FLOATING
C67 vd.n27 0 0.11fF $ **FLOATING
C68 vd.n28 0 0.22fF $ **FLOATING
C69 vd.n29 0 1.02fF $ **FLOATING
C70 vd.n30 0 1.02fF $ **FLOATING
C71 vd.n31 0 0.22fF $ **FLOATING
C72 vd.n32 0 0.11fF $ **FLOATING
C73 vd.n33 0 0.07fF $ **FLOATING
C74 vd.n34 0 0.81fF $ **FLOATING
C75 vd.n35 0 0.26fF $ **FLOATING
C76 vd.n36 0 0.10fF $ **FLOATING
C77 vd.n37 0 0.11fF $ **FLOATING
C78 vd.n38 0 0.22fF $ **FLOATING
C79 vd.n39 0 1.02fF $ **FLOATING
C80 vd.n40 0 1.02fF $ **FLOATING
C81 vd.n41 0 0.22fF $ **FLOATING
C82 vd.n42 0 1.48fF $ **FLOATING
C83 vd.n43 0 0.13fF $ **FLOATING
C84 vd.n44 0 0.11fF $ **FLOATING
C85 vd.n45 0 0.07fF $ **FLOATING
C86 vd.n46 0 1.48fF $ **FLOATING
C87 vd.n47 0 0.03fF $ **FLOATING
C88 vd.n48 0 0.12fF $ **FLOATING
C89 vd.n49 0 0.87fF $ **FLOATING
C90 ib.t1 0 0.12fF
C91 ib.t7 0 0.52fF
C92 ib.t6 0 0.62fF
C93 ib.n0 0 0.57fF $ **FLOATING
C94 ib.t4 0 0.62fF
C95 ib.n1 0 0.26fF $ **FLOATING
C96 ib.t3 0 0.62fF
C97 ib.n2 0 0.26fF $ **FLOATING
C98 ib.t5 0 0.62fF
C99 ib.n3 0 0.31fF $ **FLOATING
C100 ib.t2 0 0.52fF
C101 ib.n4 0 0.32fF $ **FLOATING
C102 ib.t0 0 0.52fF
C103 ib.n5 0 0.26fF $ **FLOATING
C104 ib.n6 0 0.34fF $ **FLOATING
C105 out.n0 0 0.93fF $ **FLOATING
C106 out.n1 0 0.02fF $ **FLOATING
C107 out.n2 0 0.07fF $ **FLOATING
C108 out.n3 0 0.93fF $ **FLOATING
C109 out.n4 0 0.08fF $ **FLOATING
C110 out.n5 0 0.07fF $ **FLOATING
C111 out.n6 0 0.14fF $ **FLOATING
C112 out.n7 0 0.64fF $ **FLOATING
C113 out.n8 0 0.64fF $ **FLOATING
C114 out.n9 0 0.14fF $ **FLOATING
C115 out.n10 0 0.07fF $ **FLOATING
C116 out.n11 0 0.04fF $ **FLOATING
C117 out.n12 0 0.42fF $ **FLOATING
C118 vs.n0 0 0.94fF $ **FLOATING
C119 vs.n1 0 0.10fF $ **FLOATING
C120 vs.n2 0 0.08fF $ **FLOATING
C121 vs.n3 0 0.18fF $ **FLOATING
C122 vs.n4 0 0.53fF $ **FLOATING
C123 vs.n5 0 0.53fF $ **FLOATING
C124 vs.n6 0 0.18fF $ **FLOATING
C125 vs.n7 0 0.08fF $ **FLOATING
C126 vs.n8 0 0.06fF $ **FLOATING
C127 vs.n9 0 0.94fF $ **FLOATING
C128 vs.n10 0 0.04fF $ **FLOATING
C129 vs.n11 0 0.13fF $ **FLOATING
C130 vs.n12 0 0.29fF $ **FLOATING
C131 vs.n13 0 0.94fF $ **FLOATING
C132 vs.n14 0 0.10fF $ **FLOATING
C133 vs.n15 0 0.08fF $ **FLOATING
C134 vs.n16 0 0.18fF $ **FLOATING
C135 vs.n17 0 0.53fF $ **FLOATING
C136 vs.n18 0 0.53fF $ **FLOATING
C137 vs.n19 0 0.18fF $ **FLOATING
C138 vs.n20 0 0.08fF $ **FLOATING
C139 vs.n21 0 0.06fF $ **FLOATING
C140 vs.n22 0 0.94fF $ **FLOATING
C141 vs.n23 0 0.04fF $ **FLOATING
C142 vs.n24 0 0.13fF $ **FLOATING
C143 vs.n25 0 0.29fF $ **FLOATING
C144 vs.n26 0 9.30fF $ **FLOATING
C145 vs.n27 0 2.86fF $ **FLOATING
C146 vs.n28 0 0.47fF $ **FLOATING
C147 vs.n29 0 0.23fF $ **FLOATING
C148 vd 0 27.83fF
C149 ib 0 -31.45fF
C150 vs 0 21.62fF
C151 c 0 -2.70fF
C152 in2 0 0.40fF
C153 in1 0 1.82fF
C154 out 0 5.47fF
C155 e 0 2.80fF
C156 d 0 16.90fF


**** end user architecture code
XM5 ib ib vd vd sky130_fd_pr__pfet_01v8 L=1 W=6 nf=1 ad='int((nf+1)/2) * W/nf * 0.29' as='int((nf+2)/2) * W/nf * 0.29'
+ pd='2*int((nf+1)/2) * (W/nf + 0.29)' ps='2*int((nf+2)/2) * (W/nf + 0.29)' nrd='0.29 / W' nrs='0.29 / W'
+ sa=0 sb=0 sd=0 mult=1 m=1
XM6 b ib vd vd sky130_fd_pr__pfet_01v8 L=1 W=6 nf=1 ad='int((nf+1)/2) * W/nf * 0.29' as='int((nf+2)/2) * W/nf * 0.29'
+ pd='2*int((nf+1)/2) * (W/nf + 0.29)' ps='2*int((nf+2)/2) * (W/nf + 0.29)' nrd='0.29 / W' nrs='0.29 / W'
+ sa=0 sb=0 sd=0 mult=1 m=1
XM8 out ib vd vd sky130_fd_pr__pfet_01v8 L=1 W=30 nf=4 ad='int((nf+1)/2) * W/nf * 0.29' as='int((nf+2)/2) * W/nf * 0.29'
+ pd='2*int((nf+1)/2) * (W/nf + 0.29)' ps='2*int((nf+2)/2) * (W/nf + 0.29)' nrd='0.29 / W' nrs='0.29 / W'
+ sa=0 sb=0 sd=0 mult=1 m=1
XM1 c in1 b b sky130_fd_pr__pfet_01v8 L=1 W=3 nf=1 ad='int((nf+1)/2) * W/nf * 0.29' as='int((nf+2)/2) * W/nf * 0.29'
+ pd='2*int((nf+1)/2) * (W/nf + 0.29)' ps='2*int((nf+2)/2) * (W/nf + 0.29)' nrd='0.29 / W' nrs='0.29 / W'
+ sa=0 sb=0 sd=0 mult=1 m=1
XM2 d in2 b b sky130_fd_pr__pfet_01v8 L=1 W=3 nf=1 ad='int((nf+1)/2) * W/nf * 0.29' as='int((nf+2)/2) * W/nf * 0.29'
+ pd='2*int((nf+1)/2) * (W/nf + 0.29)' ps='2*int((nf+2)/2) * (W/nf + 0.29)' nrd='0.29 / W' nrs='0.29 / W'
+ sa=0 sb=0 sd=0 mult=1 m=1
XM3 c c vs vs sky130_fd_pr__nfet_01v8 L=1 W=1 nf=1 ad='int((nf+1)/2) * W/nf * 0.29' as='int((nf+2)/2) * W/nf * 0.29'
+ pd='2*int((nf+1)/2) * (W/nf + 0.29)' ps='2*int((nf+2)/2) * (W/nf + 0.29)' nrd='0.29 / W' nrs='0.29 / W'
+ sa=0 sb=0 sd=0 mult=1 m=1
XM4 d c vs vs sky130_fd_pr__nfet_01v8 L=1 W=1 nf=1 ad='int((nf+1)/2) * W/nf * 0.29' as='int((nf+2)/2) * W/nf * 0.29'
+ pd='2*int((nf+1)/2) * (W/nf + 0.29)' ps='2*int((nf+2)/2) * (W/nf + 0.29)' nrd='0.29 / W' nrs='0.29 / W'
+ sa=0 sb=0 sd=0 mult=1 m=1
XM7 out d vs vs sky130_fd_pr__nfet_01v8 L=1 W=9 nf=2 ad='int((nf+1)/2) * W/nf * 0.29' as='int((nf+2)/2) * W/nf * 0.29'
+ pd='2*int((nf+1)/2) * (W/nf + 0.29)' ps='2*int((nf+2)/2) * (W/nf + 0.29)' nrd='0.29 / W' nrs='0.29 / W'
+ sa=0 sb=0 sd=0 mult=1 m=1
.ends

.GLOBAL GND
.end
